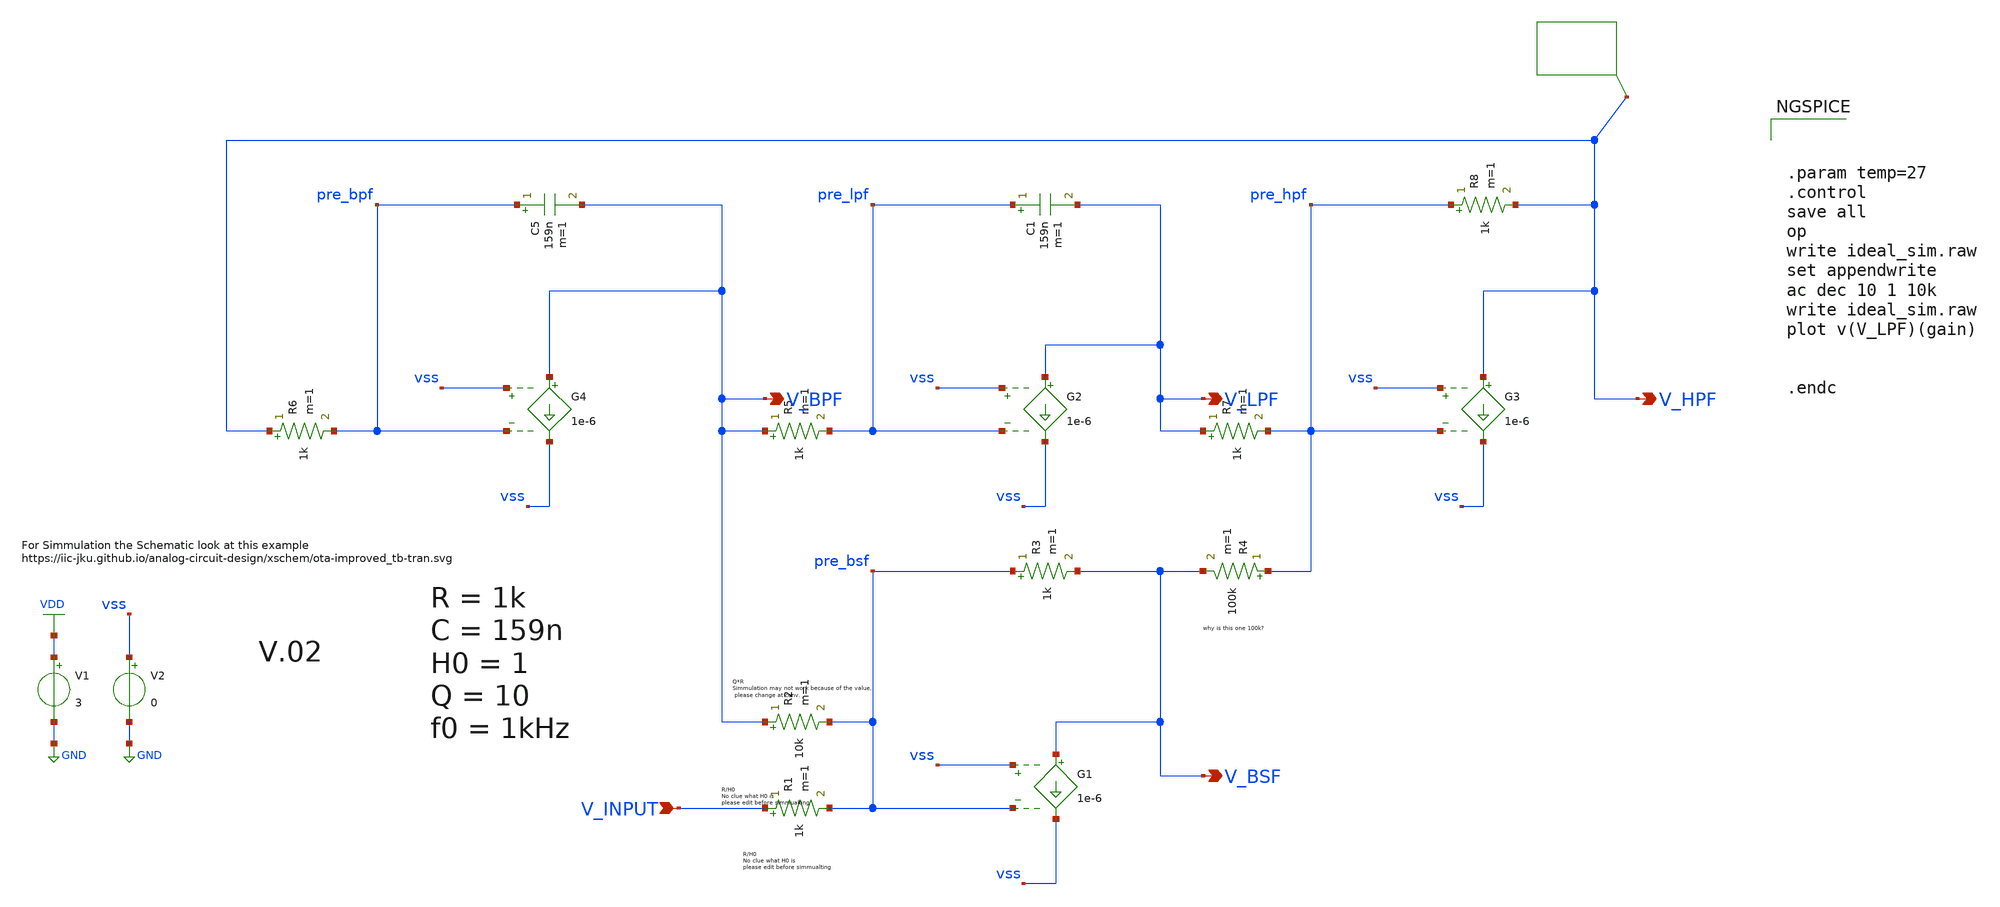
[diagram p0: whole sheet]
** sch_path: 2_Ideal_Cir/Top_Level_Ideal.sch
**.subckt Top_Level_Ideal V_BPF V_LPF V_HPF V_BSF V_INPUT
*.opin V_BPF
*.opin V_LPF
*.opin V_HPF
*.opin V_BSF
*.ipin V_INPUT
G1 V_BSF vss vss pre_bsf 1e-6
R1 V_INPUT pre_bsf 1k m=1
R2 V_BPF pre_bsf 10k m=1
R3 pre_bsf V_BSF 1k m=1
R4 pre_hpf V_BSF 100k m=1
R5 V_BPF pre_lpf 1k m=1
R6 V_HPF pre_bpf 1k m=1
C5 pre_bpf V_BPF 159n m=1
R7 V_LPF pre_hpf 1k m=1
R8 pre_hpf V_HPF 1k m=1
C1 pre_lpf V_LPF 159n m=1
V1 VDD GND 3
V2 vss GND 0
G2 V_LPF vss vss pre_lpf 1e-6
G3 V_HPF vss vss pre_hpf 1e-6
G4 V_BPF vss vss pre_bpf 1e-6
**** begin user architecture code



.param temp=27
.control
save all
op
write ideal_sim.raw
set appendwrite
ac dec 10 1 10k
write ideal_sim.raw
plot v(V_LPF)(gain)


.endc


**** end user architecture code
**.ends
.GLOBAL VDD
.GLOBAL GND
.end
